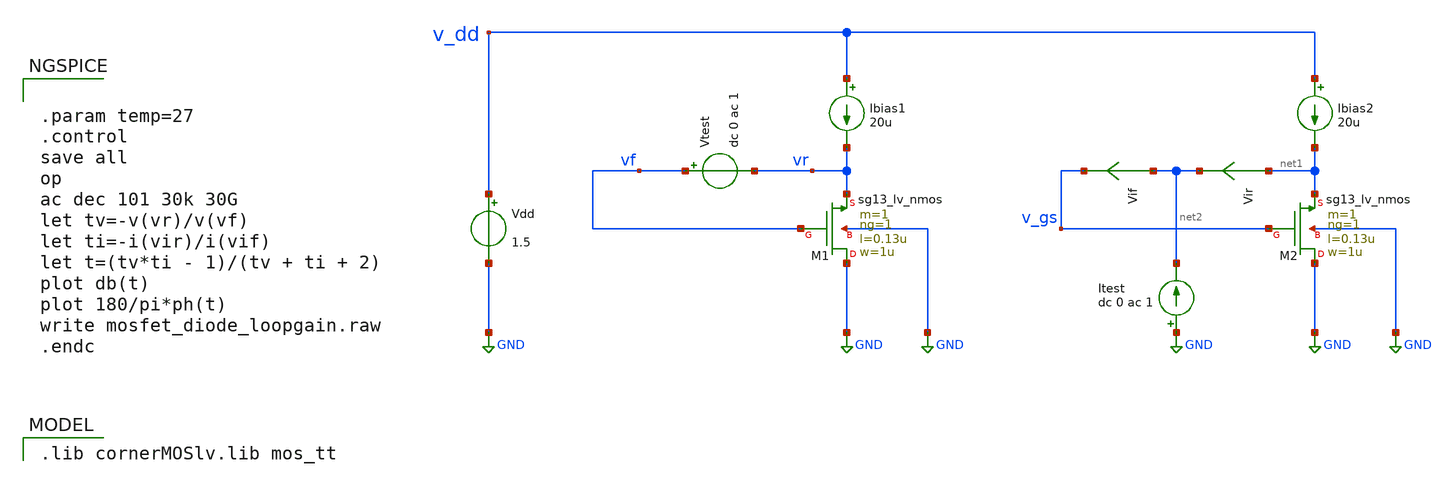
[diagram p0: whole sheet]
** sch_path: xschem/mosfet_diode_loopgain.sch
* Copyright 2024 Harald Pretl
**.subckt mosfet_diode_loopgain
Vdd v_dd GND 1.5
XM1 GND vf vr GND sg13_lv_nmos w=1u l=0.13u ng=1 m=1 mm_ok=1
Ibias1 v_dd vr 20u
Vtest vf vr dc 0 ac 1
XM2 GND v_gs net1 GND sg13_lv_nmos w=1u l=0.13u ng=1 m=1 mm_ok=1
Ibias2 v_dd net1 20u
Vir net1 net2 0
.save i(vir)
Vif net2 v_gs 0
.save i(vif)
Itest GND net2 dc 0 ac 1
**** begin user architecture code
 .lib cornerMOSlv.lib mos_tt



.param temp=27
.control
save all
op
ac dec 101 30k 30G
let tv=-v(vr)/v(vf)
let ti=-i(vir)/i(vif)
let t=(tv*ti - 1)/(tv + ti + 2)
plot db(t)
plot 180/pi*ph(t)
write mosfet_diode_loopgain.raw
.endc


**** end user architecture code
**.ends
.GLOBAL GND
.end
